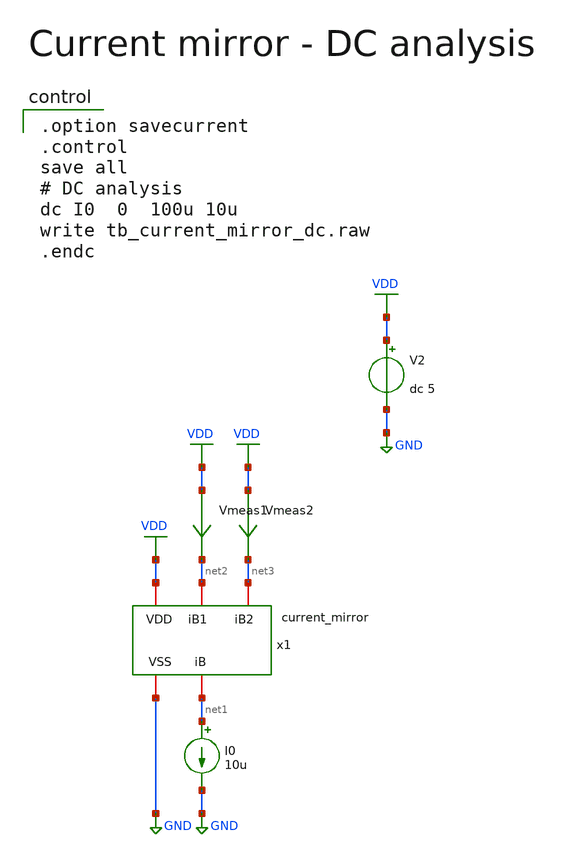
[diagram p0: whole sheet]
** sch_path: member_project/AM_Radio/Yamada3/xschem/tb_current_mirror_dc.sch
**.subckt tb_current_mirror_dc
V2 VDD GND dc 5
I0 net1 GND 10u
x1 VDD GND net1 net2 net3 current_mirror
Vmeas2 VDD net3 0
.save i(vmeas2)
Vmeas1 VDD net2 0
.save i(vmeas1)
**** begin user architecture code

.option savecurrent
.control
save all
# DC analysis
dc I0  0  100u 10u
write tb_current_mirror_dc.raw
.endc

 .include $::LIB/ip62_models
**** end user architecture code
**.ends

* expanding   symbol:  current_mirror.sym # of pins=5
** sym_path: member_project/AM_Radio/Yamada3/xschem/current_mirror.sym
** sch_path: member_project/AM_Radio/Yamada3/xschem/current_mirror.sch
.subckt current_mirror VDD VSS iB iB1 iB2
*.iopin VDD
*.iopin VSS
*.iopin iB
*.iopin iB1
*.iopin iB2
MM13 VB2 VB2 VB1 VSS NMOS w=10u l=1u as=0 ad=0 ps=0 pd=0 nrd=0 nrs=0 m=1
MM14 VB1 VB1 VSS VSS NMOS w=10u l=1u as=0 ad=0 ps=0 pd=0 nrd=0 nrs=0 m=1
MM23 VB4 VB4 VDD VDD PMOS w=30u l=1u as=0 ad=0 ps=0 pd=0 nrd=0 nrs=0 m=1
MM24 VB2 iB net1 VDD PMOS w=30u l=1u as=0 ad=0 ps=0 pd=0 nrd=0 nrs=0 m=1
MM25 net1 VB4 VDD VDD PMOS w=30u l=1u as=0 ad=0 ps=0 pd=0 nrd=0 nrs=0 m=1
MM26 iB iB VB4 VDD PMOS w=30u l=1u as=0 ad=0 ps=0 pd=0 nrd=0 nrs=0 m=1
MM1 iB1 VB2 net2 VSS NMOS w=10u l=1u as=0 ad=0 ps=0 pd=0 nrd=0 nrs=0 m=1
MM2 net2 VB1 VSS VSS NMOS w=10u l=1u as=0 ad=0 ps=0 pd=0 nrd=0 nrs=0 m=1
MM3 net4 VB2 net3 VSS NMOS w=10u l=1u as=0 ad=0 ps=0 pd=0 nrd=0 nrs=0 m=1
MM4 net3 VB1 VSS VSS NMOS w=10u l=1u as=0 ad=0 ps=0 pd=0 nrd=0 nrs=0 m=1
.ends

.GLOBAL VDD
.GLOBAL GND
.end
